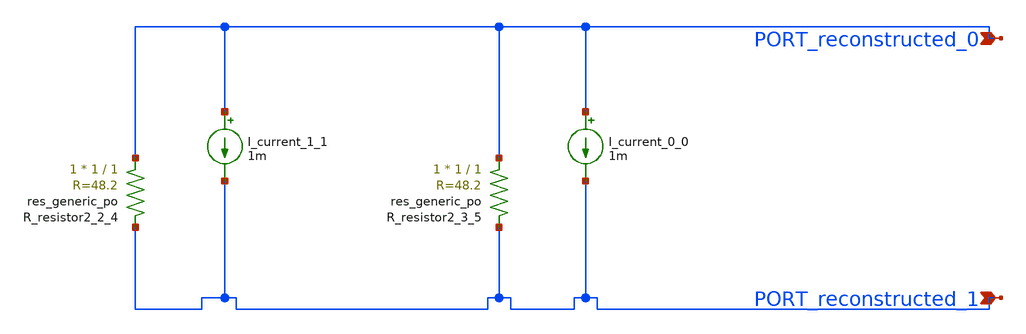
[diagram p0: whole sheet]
** sch_path: schematics/AMSNet/432.sch
**.subckt 432 PORT_reconstructed_1 PORT_reconstructed_0
*.ipin PORT_reconstructed_1
*.ipin PORT_reconstructed_0
I_current_0_0 PORT_reconstructed_0 PORT_reconstructed_1 1m
I_current_1_1 PORT_reconstructed_0 PORT_reconstructed_1 1m
XR_resistor2_2_4 PORT_reconstructed_0 PORT_reconstructed_1 sky130_fd_pr__res_generic_po W=1 L=1 m=1
XR_resistor2_3_5 PORT_reconstructed_0 PORT_reconstructed_1 sky130_fd_pr__res_generic_po W=1 L=1 m=1
**.ends
.end
